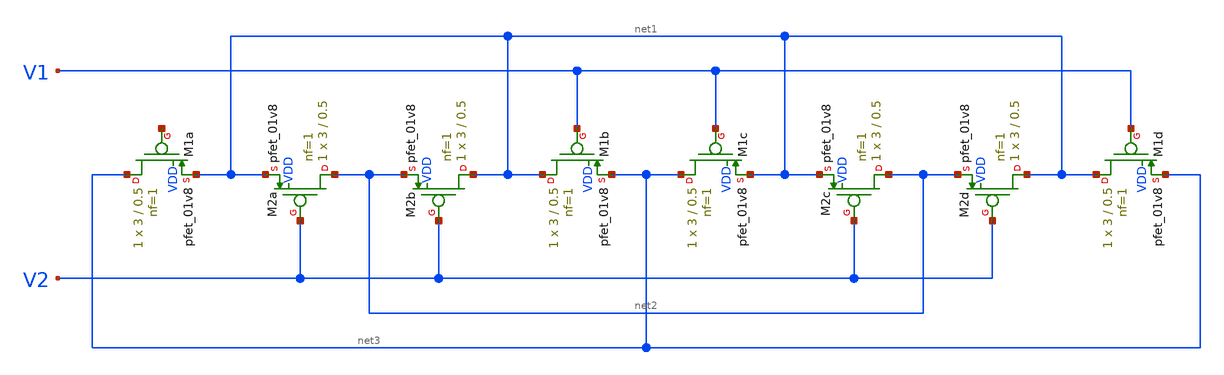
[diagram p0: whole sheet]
** sch_path: projects/current_mirror_diff_amp/xschem_ngspice/cmdiffamp.sch
**.subckt cmdiffamp
XM1a net3 net4 net1 VDD sky130_fd_pr__pfet_01v8 L=0.5 W=3 nf=1 ad='int((nf+1)/2) * W/nf * 0.29' as='int((nf+2)/2) * W/nf * 0.29'
+ pd='2*int((nf+1)/2) * (W/nf + 0.29)' ps='2*int((nf+2)/2) * (W/nf + 0.29)' nrd='0.29 / W' nrs='0.29 / W'
+ sa=0 sb=0 sd=0 mult=1 m=1
XM2a net2 V2 net1 VDD sky130_fd_pr__pfet_01v8 L=0.5 W=3 nf=1 ad='int((nf+1)/2) * W/nf * 0.29' as='int((nf+2)/2) * W/nf * 0.29'
+ pd='2*int((nf+1)/2) * (W/nf + 0.29)' ps='2*int((nf+2)/2) * (W/nf + 0.29)' nrd='0.29 / W' nrs='0.29 / W'
+ sa=0 sb=0 sd=0 mult=1 m=1
XM2b net1 V2 net2 VDD sky130_fd_pr__pfet_01v8 L=0.5 W=3 nf=1 ad='int((nf+1)/2) * W/nf * 0.29' as='int((nf+2)/2) * W/nf * 0.29'
+ pd='2*int((nf+1)/2) * (W/nf + 0.29)' ps='2*int((nf+2)/2) * (W/nf + 0.29)' nrd='0.29 / W' nrs='0.29 / W'
+ sa=0 sb=0 sd=0 mult=1 m=1
XM1b net1 V1 net3 VDD sky130_fd_pr__pfet_01v8 L=0.5 W=3 nf=1 ad='int((nf+1)/2) * W/nf * 0.29' as='int((nf+2)/2) * W/nf * 0.29'
+ pd='2*int((nf+1)/2) * (W/nf + 0.29)' ps='2*int((nf+2)/2) * (W/nf + 0.29)' nrd='0.29 / W' nrs='0.29 / W'
+ sa=0 sb=0 sd=0 mult=1 m=1
XM1c net3 V1 net1 VDD sky130_fd_pr__pfet_01v8 L=0.5 W=3 nf=1 ad='int((nf+1)/2) * W/nf * 0.29' as='int((nf+2)/2) * W/nf * 0.29'
+ pd='2*int((nf+1)/2) * (W/nf + 0.29)' ps='2*int((nf+2)/2) * (W/nf + 0.29)' nrd='0.29 / W' nrs='0.29 / W'
+ sa=0 sb=0 sd=0 mult=1 m=1
XM2c net2 V2 net1 VDD sky130_fd_pr__pfet_01v8 L=0.5 W=3 nf=1 ad='int((nf+1)/2) * W/nf * 0.29' as='int((nf+2)/2) * W/nf * 0.29'
+ pd='2*int((nf+1)/2) * (W/nf + 0.29)' ps='2*int((nf+2)/2) * (W/nf + 0.29)' nrd='0.29 / W' nrs='0.29 / W'
+ sa=0 sb=0 sd=0 mult=1 m=1
XM2d net1 V2 net2 VDD sky130_fd_pr__pfet_01v8 L=0.5 W=3 nf=1 ad='int((nf+1)/2) * W/nf * 0.29' as='int((nf+2)/2) * W/nf * 0.29'
+ pd='2*int((nf+1)/2) * (W/nf + 0.29)' ps='2*int((nf+2)/2) * (W/nf + 0.29)' nrd='0.29 / W' nrs='0.29 / W'
+ sa=0 sb=0 sd=0 mult=1 m=1
XM1d net1 V1 net3 VDD sky130_fd_pr__pfet_01v8 L=0.5 W=3 nf=1 ad='int((nf+1)/2) * W/nf * 0.29' as='int((nf+2)/2) * W/nf * 0.29'
+ pd='2*int((nf+1)/2) * (W/nf + 0.29)' ps='2*int((nf+2)/2) * (W/nf + 0.29)' nrd='0.29 / W' nrs='0.29 / W'
+ sa=0 sb=0 sd=0 mult=1 m=1
**.ends
.end
